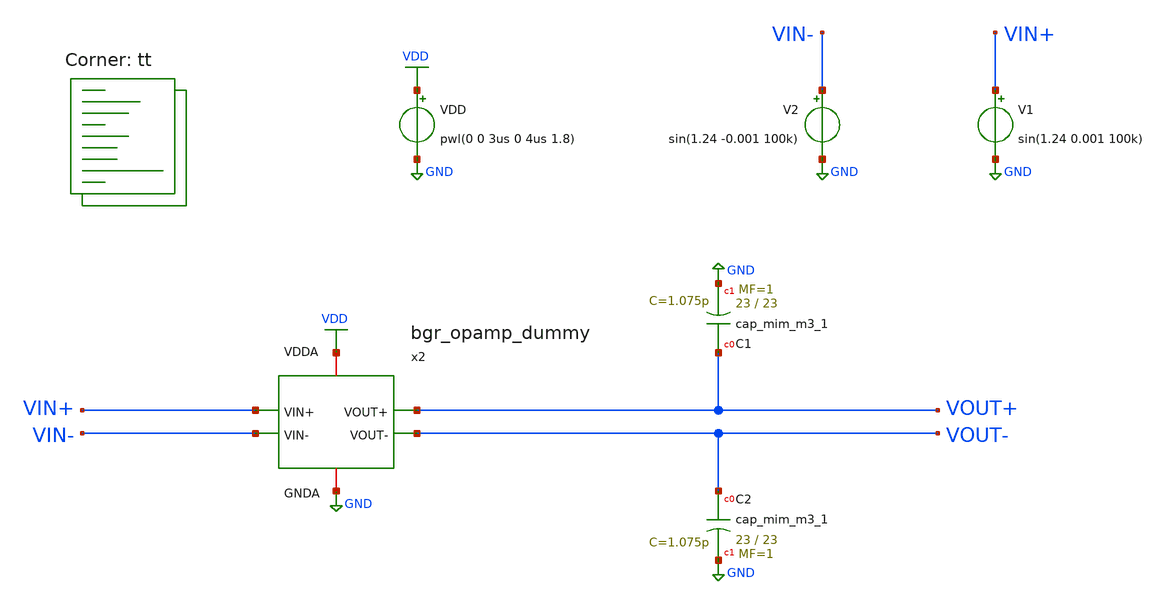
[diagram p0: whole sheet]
** sch_path: projects/opamp/xschem_ngspice/tb_bgr_opamp_dummy.sch
**.subckt tb_bgr_opamp_dummy
VDD VDD GND pwl(0 0 3us 0 4us 1.8)
V2 VIN- GND sin(1.24 -0.001 100k)
V1 VIN+ GND sin(1.24 0.001 100k)
XC1 VOUT+ GND sky130_fd_pr__cap_mim_m3_1 W=23 L=23 MF=1 m=1
XC2 VOUT- GND sky130_fd_pr__cap_mim_m3_1 W=23 L=23 MF=1 m=1
x2 VDD GND VOUT+ VOUT- VIN+ VIN- bgr_opamp_dummy
**** begin user architecture code
.lib $::SKYWATER_MODELS/sky130.lib.spice tt




.option method=gear
.option wnflag=1
.option savecurrents

.save @m.x2.xm25.msky130_fd_pr__nfet_01v8[vth] @m.x2.xm26.msky130_fd_pr__pfet_01v8[vth] @m.x2.xm27.msky130_fd_pr__nfet_01v8[vth] @m.x2.xm28.msky130_fd_pr__pfet_01v8[vth] v(vout+)  v(vout-)  v(vin+)  v(vin-)   v(x2.v_err_amp_ref) v(x2.x)  v(x2.y)  v(x2.vb1)  v(x2.vb2)  v(x2.vb3) v(x2.v_cmfb_s1) v(x2.v_cmfb_s2) v(x2.v_cmfb_s3) v(x2.v_cmfb_s4)   v(x2.v_tot)

* .ic v(v_top) = 1.8

.control

  * let runs=3
  * let run=1

  * dowhile run <= runs
    * save v(vout+) v(vout-) v(vin+) v(vin-) v(v_err_amp_ref) v(x2.x) v(x2.y) v(x2.vb1) v(x2.vb2)
+ v(x2.vb3) v(x2.v_tot)
    save all
    remzerovec
    set appendwrite
    * dc temp -40 120 10 VDD 0 4.0 0.2
    * dc VDD 0 2.0 0.02 temp -40 120 40
    * dc V5 0 0.01 0.0001
    tran 2n 30u
    * tran 1p 3n
    * tran 0.1ns 30us
    * ac dec 40 1 10T
    write tb_bgr_opamp_dummy.raw
    * write tb_bgr_opamp_dummy_2.raw
    * write tb_bgr_opamp_dummy_3.raw
    * write tb_bgr_opamp_dummy_4.raw
    * write tb_bgr_opamp_dummy_5.raw
    * write tb_bgr_opamp_dummy_6.raw
    * write tb_bgr_opamp_dummy_mc.raw
    * write tb_bgr_opamp_dummy_tt_mm.raw
    * write tb_bgr_opamp_dummy_AC.raw
    * reset
    * let run = run + 1
  * end
.endc




**** end user architecture code
**.ends

* expanding   symbol:  bgr_opamp_dummy.sym # of pins=6
** sym_path: projects/opamp/xschem_ngspice/bgr_opamp_dummy.sym
** sch_path: projects/opamp/xschem_ngspice/bgr_opamp_dummy.sch
.subckt bgr_opamp_dummy VDDA GNDA VOUT+ VOUT- VIN+ VIN-
*.ipin VIN-
*.ipin VIN+
*.opin VOUT+
*.opin VOUT-
*.iopin GNDA
*.iopin VDDA
XM7 VD1 VIN- V_p GNDA sky130_fd_pr__nfet_01v8 L=0.15 W=15 nf=1 ad='int((nf+1)/2) * W/nf * 0.29' as='int((nf+2)/2) * W/nf * 0.29'
+ pd='2*int((nf+1)/2) * (W/nf + 0.29)' ps='2*int((nf+2)/2) * (W/nf + 0.29)' nrd='0.29 / W' nrs='0.29 / W'
+ sa=0 sb=0 sd=0 mult=1 m=1
XM8 VD2 VIN+ V_p GNDA sky130_fd_pr__nfet_01v8 L=0.15 W=15 nf=1 ad='int((nf+1)/2) * W/nf * 0.29' as='int((nf+2)/2) * W/nf * 0.29'
+ pd='2*int((nf+1)/2) * (W/nf + 0.29)' ps='2*int((nf+2)/2) * (W/nf + 0.29)' nrd='0.29 / W' nrs='0.29 / W'
+ sa=0 sb=0 sd=0 mult=1 m=1
XM9 X Vb1 VD1 GNDA sky130_fd_pr__nfet_01v8 L=0.15 W=15 nf=1 ad='int((nf+1)/2) * W/nf * 0.29' as='int((nf+2)/2) * W/nf * 0.29'
+ pd='2*int((nf+1)/2) * (W/nf + 0.29)' ps='2*int((nf+2)/2) * (W/nf + 0.29)' nrd='0.29 / W' nrs='0.29 / W'
+ sa=0 sb=0 sd=0 mult=1 m=1
XM10 Y Vb1 VD2 GNDA sky130_fd_pr__nfet_01v8 L=0.15 W=15 nf=1 ad='int((nf+1)/2) * W/nf * 0.29' as='int((nf+2)/2) * W/nf * 0.29'
+ pd='2*int((nf+1)/2) * (W/nf + 0.29)' ps='2*int((nf+2)/2) * (W/nf + 0.29)' nrd='0.29 / W' nrs='0.29 / W'
+ sa=0 sb=0 sd=0 mult=1 m=1
XM11 X Vb2 VD3 VD3 sky130_fd_pr__pfet_01v8 L=0.2 W=35 nf=1 ad='int((nf+1)/2) * W/nf * 0.29' as='int((nf+2)/2) * W/nf * 0.29'
+ pd='2*int((nf+1)/2) * (W/nf + 0.29)' ps='2*int((nf+2)/2) * (W/nf + 0.29)' nrd='0.29 / W' nrs='0.29 / W'
+ sa=0 sb=0 sd=0 mult=1 m=1
XM12 Y Vb2 VD4 VD4 sky130_fd_pr__pfet_01v8 L=0.2 W=35 nf=1 ad='int((nf+1)/2) * W/nf * 0.29' as='int((nf+2)/2) * W/nf * 0.29'
+ pd='2*int((nf+1)/2) * (W/nf + 0.29)' ps='2*int((nf+2)/2) * (W/nf + 0.29)' nrd='0.29 / W' nrs='0.29 / W'
+ sa=0 sb=0 sd=0 mult=1 m=1
XM13 VD3 Vb3 VDDA VDDA sky130_fd_pr__pfet_01v8 L=0.2 W=35 nf=1 ad='int((nf+1)/2) * W/nf * 0.29' as='int((nf+2)/2) * W/nf * 0.29'
+ pd='2*int((nf+1)/2) * (W/nf + 0.29)' ps='2*int((nf+2)/2) * (W/nf + 0.29)' nrd='0.29 / W' nrs='0.29 / W'
+ sa=0 sb=0 sd=0 mult=1 m=1
XM14 VD4 Vb3 VDDA VDDA sky130_fd_pr__pfet_01v8 L=0.2 W=35 nf=1 ad='int((nf+1)/2) * W/nf * 0.29' as='int((nf+2)/2) * W/nf * 0.29'
+ pd='2*int((nf+1)/2) * (W/nf + 0.29)' ps='2*int((nf+2)/2) * (W/nf + 0.29)' nrd='0.29 / W' nrs='0.29 / W'
+ sa=0 sb=0 sd=0 mult=1 m=1
XM15 V_p V_tail_gate GNDA GNDA sky130_fd_pr__nfet_01v8 L=0.15 W=2.5 nf=1 ad='int((nf+1)/2) * W/nf * 0.29'
+ as='int((nf+2)/2) * W/nf * 0.29' pd='2*int((nf+1)/2) * (W/nf + 0.29)' ps='2*int((nf+2)/2) * (W/nf + 0.29)'
+ nrd='0.29 / W' nrs='0.29 / W' sa=0 sb=0 sd=0 mult=18 m=18
XM16 V_p_mir V_tail_gate GNDA GNDA sky130_fd_pr__nfet_01v8 L=0.15 W=2.5 nf=1 ad='int((nf+1)/2) * W/nf * 0.29'
+ as='int((nf+2)/2) * W/nf * 0.29' pd='2*int((nf+1)/2) * (W/nf + 0.29)' ps='2*int((nf+2)/2) * (W/nf + 0.29)'
+ nrd='0.29 / W' nrs='0.29 / W' sa=0 sb=0 sd=0 mult=2 m=2
XM17 V_tail_gate VIN+ V_p_mir GNDA sky130_fd_pr__nfet_01v8 L=0.15 W=1.5 nf=1 ad='int((nf+1)/2) * W/nf * 0.29'
+ as='int((nf+2)/2) * W/nf * 0.29' pd='2*int((nf+1)/2) * (W/nf + 0.29)' ps='2*int((nf+2)/2) * (W/nf + 0.29)'
+ nrd='0.29 / W' nrs='0.29 / W' sa=0 sb=0 sd=0 mult=1 m=1
XM18 V_tail_gate VIN- V_p_mir GNDA sky130_fd_pr__nfet_01v8 L=0.15 W=1.5 nf=1 ad='int((nf+1)/2) * W/nf * 0.29'
+ as='int((nf+2)/2) * W/nf * 0.29' pd='2*int((nf+1)/2) * (W/nf + 0.29)' ps='2*int((nf+2)/2) * (W/nf + 0.29)'
+ nrd='0.29 / W' nrs='0.29 / W' sa=0 sb=0 sd=0 mult=1 m=1
XM19 Vb1 Vb1 V_p GNDA sky130_fd_pr__nfet_01v8 L=2.9 W=1 nf=1 ad='int((nf+1)/2) * W/nf * 0.29' as='int((nf+2)/2) * W/nf * 0.29'
+ pd='2*int((nf+1)/2) * (W/nf + 0.29)' ps='2*int((nf+2)/2) * (W/nf + 0.29)' nrd='0.29 / W' nrs='0.29 / W'
+ sa=0 sb=0 sd=0 mult=1 m=1
XM25 VDDA X V_CMFB_S2 GNDA sky130_fd_pr__nfet_01v8 L=0.15 W=30 nf=1 ad='int((nf+1)/2) * W/nf * 0.29'
+ as='int((nf+2)/2) * W/nf * 0.29' pd='2*int((nf+1)/2) * (W/nf + 0.29)' ps='2*int((nf+2)/2) * (W/nf + 0.29)'
+ nrd='0.29 / W' nrs='0.29 / W' sa=0 sb=0 sd=0 mult=1 m=1
XM26 GNDA X V_CMFB_S1 VDDA sky130_fd_pr__pfet_01v8 L=0.15 W=20 nf=1 ad='int((nf+1)/2) * W/nf * 0.29'
+ as='int((nf+2)/2) * W/nf * 0.29' pd='2*int((nf+1)/2) * (W/nf + 0.29)' ps='2*int((nf+2)/2) * (W/nf + 0.29)'
+ nrd='0.29 / W' nrs='0.29 / W' sa=0 sb=0 sd=0 mult=1 m=1
XR10 V_CMFB_S1 V_tot GNDA sky130_fd_pr__res_xhigh_po_0p35 L=3.5 mult=1 m=1
XR11 V_CMFB_S2 V_tot GNDA sky130_fd_pr__res_xhigh_po_0p35 L=3.5 mult=1 m=1
XR12 V_CMFB_S3 V_tot GNDA sky130_fd_pr__res_xhigh_po_0p35 L=3.5 mult=1 m=1
XR13 V_CMFB_S4 V_tot GNDA sky130_fd_pr__res_xhigh_po_0p35 L=3.5 mult=1 m=1
XM27 VDDA Y V_CMFB_S4 GNDA sky130_fd_pr__nfet_01v8 L=0.15 W=30 nf=1 ad='int((nf+1)/2) * W/nf * 0.29'
+ as='int((nf+2)/2) * W/nf * 0.29' pd='2*int((nf+1)/2) * (W/nf + 0.29)' ps='2*int((nf+2)/2) * (W/nf + 0.29)'
+ nrd='0.29 / W' nrs='0.29 / W' sa=0 sb=0 sd=0 mult=1 m=1
XM28 GNDA Y V_CMFB_S3 VDDA sky130_fd_pr__pfet_01v8 L=0.15 W=20 nf=1 ad='int((nf+1)/2) * W/nf * 0.29'
+ as='int((nf+2)/2) * W/nf * 0.29' pd='2*int((nf+1)/2) * (W/nf + 0.29)' ps='2*int((nf+2)/2) * (W/nf + 0.29)'
+ nrd='0.29 / W' nrs='0.29 / W' sa=0 sb=0 sd=0 mult=1 m=1
XM29 err_amp_mir V_tot V_err_p VDDA sky130_fd_pr__pfet_01v8 L=0.15 W=2.5 nf=1 ad='int((nf+1)/2) * W/nf * 0.29'
+ as='int((nf+2)/2) * W/nf * 0.29' pd='2*int((nf+1)/2) * (W/nf + 0.29)' ps='2*int((nf+2)/2) * (W/nf + 0.29)'
+ nrd='0.29 / W' nrs='0.29 / W' sa=0 sb=0 sd=0 mult=1 m=1
XM30 err_amp_out V_err_amp_ref V_err_p VDDA sky130_fd_pr__pfet_01v8 L=0.15 W=2.5 nf=1 ad='int((nf+1)/2) * W/nf * 0.29'
+ as='int((nf+2)/2) * W/nf * 0.29' pd='2*int((nf+1)/2) * (W/nf + 0.29)' ps='2*int((nf+2)/2) * (W/nf + 0.29)'
+ nrd='0.29 / W' nrs='0.29 / W' sa=0 sb=0 sd=0 mult=1 m=1
XM31 err_amp_mir err_amp_mir GNDA GNDA sky130_fd_pr__nfet_01v8 L=0.15 W=2.5 nf=1 ad='int((nf+1)/2) * W/nf * 0.29'
+ as='int((nf+2)/2) * W/nf * 0.29' pd='2*int((nf+1)/2) * (W/nf + 0.29)' ps='2*int((nf+2)/2) * (W/nf + 0.29)'
+ nrd='0.29 / W' nrs='0.29 / W' sa=0 sb=0 sd=0 mult=1 m=1
XM32 err_amp_out err_amp_mir GNDA GNDA sky130_fd_pr__nfet_01v8 L=0.15 W=2.5 nf=1 ad='int((nf+1)/2) * W/nf * 0.29'
+ as='int((nf+2)/2) * W/nf * 0.29' pd='2*int((nf+1)/2) * (W/nf + 0.29)' ps='2*int((nf+2)/2) * (W/nf + 0.29)'
+ nrd='0.29 / W' nrs='0.29 / W' sa=0 sb=0 sd=0 mult=1 m=1
XM33 V_err_p V_err_gate VDDA VDDA sky130_fd_pr__pfet_01v8 L=0.15 W=5.0 nf=2 ad='int((nf+1)/2) * W/nf * 0.29'
+ as='int((nf+2)/2) * W/nf * 0.29' pd='2*int((nf+1)/2) * (W/nf + 0.29)' ps='2*int((nf+2)/2) * (W/nf + 0.29)'
+ nrd='0.29 / W' nrs='0.29 / W' sa=0 sb=0 sd=0 mult=1 m=1
XM34 V_err_gate V_tot V_err_mir_p VDDA sky130_fd_pr__pfet_01v8 L=0.15 W=2.5 nf=1 ad='int((nf+1)/2) * W/nf * 0.29'
+ as='int((nf+2)/2) * W/nf * 0.29' pd='2*int((nf+1)/2) * (W/nf + 0.29)' ps='2*int((nf+2)/2) * (W/nf + 0.29)'
+ nrd='0.29 / W' nrs='0.29 / W' sa=0 sb=0 sd=0 mult=1 m=1
XM35 V_err_gate V_err_amp_ref V_err_mir_p VDDA sky130_fd_pr__pfet_01v8 L=0.15 W=2.5 nf=1 ad='int((nf+1)/2) * W/nf * 0.29'
+ as='int((nf+2)/2) * W/nf * 0.29' pd='2*int((nf+1)/2) * (W/nf + 0.29)' ps='2*int((nf+2)/2) * (W/nf + 0.29)'
+ nrd='0.29 / W' nrs='0.29 / W' sa=0 sb=0 sd=0 mult=1 m=1
XM36 V_err_mir_p V_err_gate VDDA VDDA sky130_fd_pr__pfet_01v8 L=0.15 W=5.0 nf=2 ad='int((nf+1)/2) * W/nf * 0.29'
+ as='int((nf+2)/2) * W/nf * 0.29' pd='2*int((nf+1)/2) * (W/nf + 0.29)' ps='2*int((nf+2)/2) * (W/nf + 0.29)'
+ nrd='0.29 / W' nrs='0.29 / W' sa=0 sb=0 sd=0 mult=1 m=1
XM37 VOUT- V_b_2nd_stage GNDA GNDA sky130_fd_pr__nfet_01v8 L=0.6 W=28 nf=1 ad='int((nf+1)/2) * W/nf * 0.29'
+ as='int((nf+2)/2) * W/nf * 0.29' pd='2*int((nf+1)/2) * (W/nf + 0.29)' ps='2*int((nf+2)/2) * (W/nf + 0.29)'
+ nrd='0.29 / W' nrs='0.29 / W' sa=0 sb=0 sd=0 mult=1 m=1
XM38 VOUT+ V_b_2nd_stage GNDA GNDA sky130_fd_pr__nfet_01v8 L=0.6 W=28 nf=1 ad='int((nf+1)/2) * W/nf * 0.29'
+ as='int((nf+2)/2) * W/nf * 0.29' pd='2*int((nf+1)/2) * (W/nf + 0.29)' ps='2*int((nf+2)/2) * (W/nf + 0.29)'
+ nrd='0.29 / W' nrs='0.29 / W' sa=0 sb=0 sd=0 mult=1 m=1
XM39 VOUT- X VDDA VDDA sky130_fd_pr__pfet_01v8 L=0.15 W=60 nf=1 ad='int((nf+1)/2) * W/nf * 0.29' as='int((nf+2)/2) * W/nf * 0.29'
+ pd='2*int((nf+1)/2) * (W/nf + 0.29)' ps='2*int((nf+2)/2) * (W/nf + 0.29)' nrd='0.29 / W' nrs='0.29 / W'
+ sa=0 sb=0 sd=0 mult=1 m=1
XM40 VOUT+ Y VDDA VDDA sky130_fd_pr__pfet_01v8 L=0.15 W=60 nf=1 ad='int((nf+1)/2) * W/nf * 0.29' as='int((nf+2)/2) * W/nf * 0.29'
+ pd='2*int((nf+1)/2) * (W/nf + 0.29)' ps='2*int((nf+2)/2) * (W/nf + 0.29)' nrd='0.29 / W' nrs='0.29 / W'
+ sa=0 sb=0 sd=0 mult=1 m=1
XR22 VOUT- V_b_2nd_stage GNDA sky130_fd_pr__res_xhigh_po_0p35 L=5.25 mult=1 m=1
XR23 VOUT+ V_b_2nd_stage GNDA sky130_fd_pr__res_xhigh_po_0p35 L=5.25 mult=1 m=1
XM41 V_p err_amp_out GNDA GNDA sky130_fd_pr__nfet_01v8 L=0.15 W=2.5 nf=1 ad='int((nf+1)/2) * W/nf * 0.29'
+ as='int((nf+2)/2) * W/nf * 0.29' pd='2*int((nf+1)/2) * (W/nf + 0.29)' ps='2*int((nf+2)/2) * (W/nf + 0.29)'
+ nrd='0.29 / W' nrs='0.29 / W' sa=0 sb=0 sd=0 mult=1 m=1
XC6 VOUT+ cap_res_Y sky130_fd_pr__cap_mim_m3_1 W=2 L=2 MF=138 m=138
XC7 VOUT- cap_res_X sky130_fd_pr__cap_mim_m3_1 W=2 L=2 MF=138 m=138
XM21 GNDA GNDA GNDA GNDA sky130_fd_pr__nfet_01v8 L=0.15 W=2.5 nf=1 ad='int((nf+1)/2) * W/nf * 0.29' as='int((nf+2)/2) * W/nf * 0.29'
+ pd='2*int((nf+1)/2) * (W/nf + 0.29)' ps='2*int((nf+2)/2) * (W/nf + 0.29)' nrd='0.29 / W' nrs='0.29 / W'
+ sa=0 sb=0 sd=0 mult=1 m=1
XM22 V_p GNDA GNDA GNDA sky130_fd_pr__nfet_01v8 L=0.15 W=2.5 nf=1 ad='int((nf+1)/2) * W/nf * 0.29' as='int((nf+2)/2) * W/nf * 0.29'
+ pd='2*int((nf+1)/2) * (W/nf + 0.29)' ps='2*int((nf+2)/2) * (W/nf + 0.29)' nrd='0.29 / W' nrs='0.29 / W'
+ sa=0 sb=0 sd=0 mult=1 m=1
XM23 V_tail_gate GNDA GNDA GNDA sky130_fd_pr__nfet_01v8 L=0.15 W=3.0 nf=2 ad='int((nf+1)/2) * W/nf * 0.29'
+ as='int((nf+2)/2) * W/nf * 0.29' pd='2*int((nf+1)/2) * (W/nf + 0.29)' ps='2*int((nf+2)/2) * (W/nf + 0.29)'
+ nrd='0.29 / W' nrs='0.29 / W' sa=0 sb=0 sd=0 mult=1 m=1
XM24 VD1 GNDA GNDA GNDA sky130_fd_pr__nfet_01v8 L=0.15 W=3.0 nf=2 ad='int((nf+1)/2) * W/nf * 0.29' as='int((nf+2)/2) * W/nf * 0.29'
+ pd='2*int((nf+1)/2) * (W/nf + 0.29)' ps='2*int((nf+2)/2) * (W/nf + 0.29)' nrd='0.29 / W' nrs='0.29 / W'
+ sa=0 sb=0 sd=0 mult=1 m=1
XM46 VD2 GNDA GNDA GNDA sky130_fd_pr__nfet_01v8 L=0.15 W=3.0 nf=2 ad='int((nf+1)/2) * W/nf * 0.29' as='int((nf+2)/2) * W/nf * 0.29'
+ pd='2*int((nf+1)/2) * (W/nf + 0.29)' ps='2*int((nf+2)/2) * (W/nf + 0.29)' nrd='0.29 / W' nrs='0.29 / W'
+ sa=0 sb=0 sd=0 mult=1 m=1
XM47 Y GNDA GNDA GNDA sky130_fd_pr__nfet_01v8 L=0.15 W=3.0 nf=2 ad='int((nf+1)/2) * W/nf * 0.29' as='int((nf+2)/2) * W/nf * 0.29'
+ pd='2*int((nf+1)/2) * (W/nf + 0.29)' ps='2*int((nf+2)/2) * (W/nf + 0.29)' nrd='0.29 / W' nrs='0.29 / W'
+ sa=0 sb=0 sd=0 mult=1 m=1
XM48 VD3 VDDA VDDA VDDA sky130_fd_pr__pfet_01v8 L=0.2 W=7.0 nf=2 ad='int((nf+1)/2) * W/nf * 0.29' as='int((nf+2)/2) * W/nf * 0.29'
+ pd='2*int((nf+1)/2) * (W/nf + 0.29)' ps='2*int((nf+2)/2) * (W/nf + 0.29)' nrd='0.29 / W' nrs='0.29 / W'
+ sa=0 sb=0 sd=0 mult=1 m=1
XM49 Y VD4 VD4 VD4 sky130_fd_pr__pfet_01v8 L=0.2 W=7.0 nf=2 ad='int((nf+1)/2) * W/nf * 0.29' as='int((nf+2)/2) * W/nf * 0.29'
+ pd='2*int((nf+1)/2) * (W/nf + 0.29)' ps='2*int((nf+2)/2) * (W/nf + 0.29)' nrd='0.29 / W' nrs='0.29 / W'
+ sa=0 sb=0 sd=0 mult=1 m=1
XM52 X VD3 VD3 VD3 sky130_fd_pr__pfet_01v8 L=0.2 W=7.0 nf=2 ad='int((nf+1)/2) * W/nf * 0.29' as='int((nf+2)/2) * W/nf * 0.29'
+ pd='2*int((nf+1)/2) * (W/nf + 0.29)' ps='2*int((nf+2)/2) * (W/nf + 0.29)' nrd='0.29 / W' nrs='0.29 / W'
+ sa=0 sb=0 sd=0 mult=1 m=1
XM58 V_err_p VDDA VDDA VDDA sky130_fd_pr__pfet_01v8 L=0.15 W=1.0 nf=2 ad='int((nf+1)/2) * W/nf * 0.29'
+ as='int((nf+2)/2) * W/nf * 0.29' pd='2*int((nf+1)/2) * (W/nf + 0.29)' ps='2*int((nf+2)/2) * (W/nf + 0.29)'
+ nrd='0.29 / W' nrs='0.29 / W' sa=0 sb=0 sd=0 mult=1 m=1
XM59 err_amp_out VDDA VDDA VDDA sky130_fd_pr__pfet_01v8 L=0.15 W=0.5 nf=1 ad='int((nf+1)/2) * W/nf * 0.29'
+ as='int((nf+2)/2) * W/nf * 0.29' pd='2*int((nf+1)/2) * (W/nf + 0.29)' ps='2*int((nf+2)/2) * (W/nf + 0.29)'
+ nrd='0.29 / W' nrs='0.29 / W' sa=0 sb=0 sd=0 mult=1 m=1
XM60 V_err_gate VDDA VDDA VDDA sky130_fd_pr__pfet_01v8 L=0.15 W=1.0 nf=2 ad='int((nf+1)/2) * W/nf * 0.29'
+ as='int((nf+2)/2) * W/nf * 0.29' pd='2*int((nf+1)/2) * (W/nf + 0.29)' ps='2*int((nf+2)/2) * (W/nf + 0.29)'
+ nrd='0.29 / W' nrs='0.29 / W' sa=0 sb=0 sd=0 mult=1 m=1
XM61 err_amp_mir VDDA VDDA VDDA sky130_fd_pr__pfet_01v8 L=0.15 W=0.5 nf=1 ad='int((nf+1)/2) * W/nf * 0.29'
+ as='int((nf+2)/2) * W/nf * 0.29' pd='2*int((nf+1)/2) * (W/nf + 0.29)' ps='2*int((nf+2)/2) * (W/nf + 0.29)'
+ nrd='0.29 / W' nrs='0.29 / W' sa=0 sb=0 sd=0 mult=1 m=1
XM62 GNDA VDDA VDDA VDDA sky130_fd_pr__pfet_01v8 L=0.15 W=4 nf=2 ad='int((nf+1)/2) * W/nf * 0.29' as='int((nf+2)/2) * W/nf * 0.29'
+ pd='2*int((nf+1)/2) * (W/nf + 0.29)' ps='2*int((nf+2)/2) * (W/nf + 0.29)' nrd='0.29 / W' nrs='0.29 / W'
+ sa=0 sb=0 sd=0 mult=1 m=1
XM63 GNDA VDDA VDDA VDDA sky130_fd_pr__pfet_01v8 L=0.15 W=4 nf=2 ad='int((nf+1)/2) * W/nf * 0.29' as='int((nf+2)/2) * W/nf * 0.29'
+ pd='2*int((nf+1)/2) * (W/nf + 0.29)' ps='2*int((nf+2)/2) * (W/nf + 0.29)' nrd='0.29 / W' nrs='0.29 / W'
+ sa=0 sb=0 sd=0 mult=1 m=1
XM64 VDDA GNDA GNDA GNDA sky130_fd_pr__nfet_01v8 L=0.15 W=6 nf=2 ad='int((nf+1)/2) * W/nf * 0.29' as='int((nf+2)/2) * W/nf * 0.29'
+ pd='2*int((nf+1)/2) * (W/nf + 0.29)' ps='2*int((nf+2)/2) * (W/nf + 0.29)' nrd='0.29 / W' nrs='0.29 / W'
+ sa=0 sb=0 sd=0 mult=1 m=1
XM65 VDDA GNDA GNDA GNDA sky130_fd_pr__nfet_01v8 L=0.15 W=6 nf=2 ad='int((nf+1)/2) * W/nf * 0.29' as='int((nf+2)/2) * W/nf * 0.29'
+ pd='2*int((nf+1)/2) * (W/nf + 0.29)' ps='2*int((nf+2)/2) * (W/nf + 0.29)' nrd='0.29 / W' nrs='0.29 / W'
+ sa=0 sb=0 sd=0 mult=1 m=1
XM66 VOUT+ GNDA GNDA GNDA sky130_fd_pr__nfet_01v8 L=0.6 W=14 nf=2 ad='int((nf+1)/2) * W/nf * 0.29' as='int((nf+2)/2) * W/nf * 0.29'
+ pd='2*int((nf+1)/2) * (W/nf + 0.29)' ps='2*int((nf+2)/2) * (W/nf + 0.29)' nrd='0.29 / W' nrs='0.29 / W'
+ sa=0 sb=0 sd=0 mult=1 m=1
XM68 VOUT- VDDA VDDA VDDA sky130_fd_pr__pfet_01v8 L=0.15 W=12 nf=2 ad='int((nf+1)/2) * W/nf * 0.29' as='int((nf+2)/2) * W/nf * 0.29'
+ pd='2*int((nf+1)/2) * (W/nf + 0.29)' ps='2*int((nf+2)/2) * (W/nf + 0.29)' nrd='0.29 / W' nrs='0.29 / W'
+ sa=0 sb=0 sd=0 mult=1 m=1
XM69 VOUT- GNDA GNDA GNDA sky130_fd_pr__nfet_01v8 L=0.6 W=14 nf=2 ad='int((nf+1)/2) * W/nf * 0.29' as='int((nf+2)/2) * W/nf * 0.29'
+ pd='2*int((nf+1)/2) * (W/nf + 0.29)' ps='2*int((nf+2)/2) * (W/nf + 0.29)' nrd='0.29 / W' nrs='0.29 / W'
+ sa=0 sb=0 sd=0 mult=1 m=1
XM67 VOUT+ VDDA VDDA VDDA sky130_fd_pr__pfet_01v8 L=0.15 W=12 nf=2 ad='int((nf+1)/2) * W/nf * 0.29' as='int((nf+2)/2) * W/nf * 0.29'
+ pd='2*int((nf+1)/2) * (W/nf + 0.29)' ps='2*int((nf+2)/2) * (W/nf + 0.29)' nrd='0.29 / W' nrs='0.29 / W'
+ sa=0 sb=0 sd=0 mult=1 m=1
XR1 cap_res_X X GNDA sky130_fd_pr__res_high_po_1p41 L=1.41 mult=1 m=1
XR2 cap_res_Y Y GNDA sky130_fd_pr__res_high_po_1p41 L=1.41 mult=1 m=1
XM20 err_amp_mir GNDA GNDA GNDA sky130_fd_pr__nfet_01v8 L=0.15 W=0.5 nf=1 ad='int((nf+1)/2) * W/nf * 0.29'
+ as='int((nf+2)/2) * W/nf * 0.29' pd='2*int((nf+1)/2) * (W/nf + 0.29)' ps='2*int((nf+2)/2) * (W/nf + 0.29)'
+ nrd='0.29 / W' nrs='0.29 / W' sa=0 sb=0 sd=0 mult=1 m=1
XM42 err_amp_out GNDA GNDA GNDA sky130_fd_pr__nfet_01v8 L=0.15 W=0.5 nf=1 ad='int((nf+1)/2) * W/nf * 0.29'
+ as='int((nf+2)/2) * W/nf * 0.29' pd='2*int((nf+1)/2) * (W/nf + 0.29)' ps='2*int((nf+2)/2) * (W/nf + 0.29)'
+ nrd='0.29 / W' nrs='0.29 / W' sa=0 sb=0 sd=0 mult=1 m=1
XM44 X GNDA GNDA GNDA sky130_fd_pr__nfet_01v8 L=0.15 W=3.0 nf=2 ad='int((nf+1)/2) * W/nf * 0.29' as='int((nf+2)/2) * W/nf * 0.29'
+ pd='2*int((nf+1)/2) * (W/nf + 0.29)' ps='2*int((nf+2)/2) * (W/nf + 0.29)' nrd='0.29 / W' nrs='0.29 / W'
+ sa=0 sb=0 sd=0 mult=1 m=1
XM45 V_err_amp_ref V_TOP VDDA VDDA sky130_fd_pr__pfet_01v8 L=0.5 W=12 nf=4 ad='int((nf+1)/2) * W/nf * 0.29'
+ as='int((nf+2)/2) * W/nf * 0.29' pd='2*int((nf+1)/2) * (W/nf + 0.29)' ps='2*int((nf+2)/2) * (W/nf + 0.29)'
+ nrd='0.29 / W' nrs='0.29 / W' sa=0 sb=0 sd=0 mult=1 m=1
XR4 GNDA V_err_amp_ref GNDA sky130_fd_pr__res_xhigh_po_0p35 L=12.7 mult=1 m=1
XR5 GNDA V_CUR_REF_REG GNDA sky130_fd_pr__res_xhigh_po_0p35 L=12 mult=1 m=1
XM50 V_CUR_REF_REG PFET_GATE_10uA VDDA VDDA sky130_fd_pr__pfet_01v8 L=0.15 W=1 nf=1 ad='int((nf+1)/2) * W/nf * 0.29'
+ as='int((nf+2)/2) * W/nf * 0.29' pd='2*int((nf+1)/2) * (W/nf + 0.29)' ps='2*int((nf+2)/2) * (W/nf + 0.29)'
+ nrd='0.29 / W' nrs='0.29 / W' sa=0 sb=0 sd=0 mult=1 m=1
XC1 V_TOP VDDA sky130_fd_pr__cap_mim_m3_1 W=2 L=2 MF=20 m=20
XQ1 GNDA GNDA bgr_Vin- sky130_fd_pr__pnp_05v5_W3p40L3p40 m=1
XQ2 GNDA GNDA Vbe2 sky130_fd_pr__pnp_05v5_W3p40L3p40 m=8
XM51 bgr_Vin- V_TOP VDDA VDDA sky130_fd_pr__pfet_01v8 L=0.5 W=12 nf=4 ad='int((nf+1)/2) * W/nf * 0.29'
+ as='int((nf+2)/2) * W/nf * 0.29' pd='2*int((nf+1)/2) * (W/nf + 0.29)' ps='2*int((nf+2)/2) * (W/nf + 0.29)'
+ nrd='0.29 / W' nrs='0.29 / W' sa=0 sb=0 sd=0 mult=1 m=1
XM53 bgr_Vin+ V_TOP VDDA VDDA sky130_fd_pr__pfet_01v8 L=0.5 W=12 nf=4 ad='int((nf+1)/2) * W/nf * 0.29'
+ as='int((nf+2)/2) * W/nf * 0.29' pd='2*int((nf+1)/2) * (W/nf + 0.29)' ps='2*int((nf+2)/2) * (W/nf + 0.29)'
+ nrd='0.29 / W' nrs='0.29 / W' sa=0 sb=0 sd=0 mult=1 m=1
XR3 Vbe2 bgr_Vin+ GNDA sky130_fd_pr__res_xhigh_po_0p35 L=2.3 mult=1 m=1
XR6 GNDA bgr_Vin+ GNDA sky130_fd_pr__res_xhigh_po_0p35 L=18 mult=1 m=1
XR7 GNDA bgr_Vin- GNDA sky130_fd_pr__res_xhigh_po_0p35 L=18 mult=1 m=1
XM54 START_UP START_UP START_UP_NFET1 GNDA sky130_fd_pr__nfet_01v8 L=10 W=1 nf=1 ad='int((nf+1)/2) * W/nf * 0.29'
+ as='int((nf+2)/2) * W/nf * 0.29' pd='2*int((nf+1)/2) * (W/nf + 0.29)' ps='2*int((nf+2)/2) * (W/nf + 0.29)'
+ nrd='0.29 / W' nrs='0.29 / W' sa=0 sb=0 sd=0 mult=1 m=1
XM55 START_UP V_TOP VDDA VDDA sky130_fd_pr__pfet_01v8 L=0.5 W=12 nf=4 ad='int((nf+1)/2) * W/nf * 0.29'
+ as='int((nf+2)/2) * W/nf * 0.29' pd='2*int((nf+1)/2) * (W/nf + 0.29)' ps='2*int((nf+2)/2) * (W/nf + 0.29)'
+ nrd='0.29 / W' nrs='0.29 / W' sa=0 sb=0 sd=0 mult=1 m=1
XM56 bgr_Vin- START_UP V_TOP VDDA sky130_fd_pr__pfet_01v8 L=0.15 W=2 nf=2 ad='int((nf+1)/2) * W/nf * 0.29'
+ as='int((nf+2)/2) * W/nf * 0.29' pd='2*int((nf+1)/2) * (W/nf + 0.29)' ps='2*int((nf+2)/2) * (W/nf + 0.29)'
+ nrd='0.29 / W' nrs='0.29 / W' sa=0 sb=0 sd=0 mult=1 m=1
XM57 START_UP_NFET1 START_UP_NFET1 GNDA GNDA sky130_fd_pr__nfet_01v8 L=10 W=1 nf=1 ad='int((nf+1)/2) * W/nf * 0.29'
+ as='int((nf+2)/2) * W/nf * 0.29' pd='2*int((nf+1)/2) * (W/nf + 0.29)' ps='2*int((nf+2)/2) * (W/nf + 0.29)'
+ nrd='0.29 / W' nrs='0.29 / W' sa=0 sb=0 sd=0 mult=1 m=1
x1 VDDA V_TOP bgr_Vin- bgr_Vin+ GNDA opamp_bandgap_2
x2 VDDA PFET_GATE_10uA V_err_amp_ref V_CUR_REF_REG GNDA opamp_bandgap_2
XM70 NFET_GATE_10uA PFET_GATE_10uA VDDA VDDA sky130_fd_pr__pfet_01v8 L=0.15 W=1 nf=1 ad='int((nf+1)/2) * W/nf * 0.29'
+ as='int((nf+2)/2) * W/nf * 0.29' pd='2*int((nf+1)/2) * (W/nf + 0.29)' ps='2*int((nf+2)/2) * (W/nf + 0.29)'
+ nrd='0.29 / W' nrs='0.29 / W' sa=0 sb=0 sd=0 mult=1 m=1
XM71 NFET_GATE_10uA NFET_GATE_10uA GNDA GNDA sky130_fd_pr__nfet_01v8 L=0.15 W=1 nf=1 ad='int((nf+1)/2) * W/nf * 0.29'
+ as='int((nf+2)/2) * W/nf * 0.29' pd='2*int((nf+1)/2) * (W/nf + 0.29)' ps='2*int((nf+2)/2) * (W/nf + 0.29)'
+ nrd='0.29 / W' nrs='0.29 / W' sa=0 sb=0 sd=0 mult=1 m=1
XM72 Vb2 NFET_GATE_10uA GNDA GNDA sky130_fd_pr__nfet_01v8 L=0.15 W=1 nf=1 ad='int((nf+1)/2) * W/nf * 0.29'
+ as='int((nf+2)/2) * W/nf * 0.29' pd='2*int((nf+1)/2) * (W/nf + 0.29)' ps='2*int((nf+2)/2) * (W/nf + 0.29)'
+ nrd='0.29 / W' nrs='0.29 / W' sa=0 sb=0 sd=0 mult=6 m=6
XM73 Vb3 NFET_GATE_10uA GNDA GNDA sky130_fd_pr__nfet_01v8 L=0.15 W=1 nf=1 ad='int((nf+1)/2) * W/nf * 0.29'
+ as='int((nf+2)/2) * W/nf * 0.29' pd='2*int((nf+1)/2) * (W/nf + 0.29)' ps='2*int((nf+2)/2) * (W/nf + 0.29)'
+ nrd='0.29 / W' nrs='0.29 / W' sa=0 sb=0 sd=0 mult=5 m=5
XM74 Vb1 PFET_GATE_10uA VDDA VDDA sky130_fd_pr__pfet_01v8 L=0.15 W=1 nf=1 ad='int((nf+1)/2) * W/nf * 0.29'
+ as='int((nf+2)/2) * W/nf * 0.29' pd='2*int((nf+1)/2) * (W/nf + 0.29)' ps='2*int((nf+2)/2) * (W/nf + 0.29)'
+ nrd='0.29 / W' nrs='0.29 / W' sa=0 sb=0 sd=0 mult=2 m=2
XM75 V_err_gate NFET_GATE_10uA GNDA GNDA sky130_fd_pr__nfet_01v8 L=0.15 W=1 nf=1 ad='int((nf+1)/2) * W/nf * 0.29'
+ as='int((nf+2)/2) * W/nf * 0.29' pd='2*int((nf+1)/2) * (W/nf + 0.29)' ps='2*int((nf+2)/2) * (W/nf + 0.29)'
+ nrd='0.29 / W' nrs='0.29 / W' sa=0 sb=0 sd=0 mult=2 m=2
XM76 V_CMFB_S2 NFET_GATE_10uA GNDA GNDA sky130_fd_pr__nfet_01v8 L=0.15 W=1 nf=1 ad='int((nf+1)/2) * W/nf * 0.29'
+ as='int((nf+2)/2) * W/nf * 0.29' pd='2*int((nf+1)/2) * (W/nf + 0.29)' ps='2*int((nf+2)/2) * (W/nf + 0.29)'
+ nrd='0.29 / W' nrs='0.29 / W' sa=0 sb=0 sd=0 mult=3 m=3
XM77 V_tail_gate PFET_GATE_10uA VDDA VDDA sky130_fd_pr__pfet_01v8 L=0.15 W=1 nf=1 ad='int((nf+1)/2) * W/nf * 0.29'
+ as='int((nf+2)/2) * W/nf * 0.29' pd='2*int((nf+1)/2) * (W/nf + 0.29)' ps='2*int((nf+2)/2) * (W/nf + 0.29)'
+ nrd='0.29 / W' nrs='0.29 / W' sa=0 sb=0 sd=0 mult=8 m=8
XM78 NFET_GATE_10uA VDDA VDDA VDDA sky130_fd_pr__pfet_01v8 L=0.15 W=1 nf=1 ad='int((nf+1)/2) * W/nf * 0.29'
+ as='int((nf+2)/2) * W/nf * 0.29' pd='2*int((nf+1)/2) * (W/nf + 0.29)' ps='2*int((nf+2)/2) * (W/nf + 0.29)'
+ nrd='0.29 / W' nrs='0.29 / W' sa=0 sb=0 sd=0 mult=1 m=1
XM79 NFET_GATE_10uA GNDA GNDA GNDA sky130_fd_pr__nfet_01v8 L=0.15 W=1 nf=1 ad='int((nf+1)/2) * W/nf * 0.29'
+ as='int((nf+2)/2) * W/nf * 0.29' pd='2*int((nf+1)/2) * (W/nf + 0.29)' ps='2*int((nf+2)/2) * (W/nf + 0.29)'
+ nrd='0.29 / W' nrs='0.29 / W' sa=0 sb=0 sd=0 mult=1 m=1
XM80 V_CUR_REF_REG VDDA VDDA VDDA sky130_fd_pr__pfet_01v8 L=0.15 W=1 nf=1 ad='int((nf+1)/2) * W/nf * 0.29'
+ as='int((nf+2)/2) * W/nf * 0.29' pd='2*int((nf+1)/2) * (W/nf + 0.29)' ps='2*int((nf+2)/2) * (W/nf + 0.29)'
+ nrd='0.29 / W' nrs='0.29 / W' sa=0 sb=0 sd=0 mult=1 m=1
XM81 Vb3 GNDA GNDA GNDA sky130_fd_pr__nfet_01v8 L=0.15 W=1 nf=1 ad='int((nf+1)/2) * W/nf * 0.29' as='int((nf+2)/2) * W/nf * 0.29'
+ pd='2*int((nf+1)/2) * (W/nf + 0.29)' ps='2*int((nf+2)/2) * (W/nf + 0.29)' nrd='0.29 / W' nrs='0.29 / W'
+ sa=0 sb=0 sd=0 mult=1 m=1
XM82 V_CMFB_S1 PFET_GATE_10uA VDDA VDDA sky130_fd_pr__pfet_01v8 L=0.15 W=1 nf=1 ad='int((nf+1)/2) * W/nf * 0.29'
+ as='int((nf+2)/2) * W/nf * 0.29' pd='2*int((nf+1)/2) * (W/nf + 0.29)' ps='2*int((nf+2)/2) * (W/nf + 0.29)'
+ nrd='0.29 / W' nrs='0.29 / W' sa=0 sb=0 sd=0 mult=4 m=4
XM83 V_err_amp_ref VDDA VDDA VDDA sky130_fd_pr__pfet_01v8 L=0.5 W=6 nf=2 ad='int((nf+1)/2) * W/nf * 0.29'
+ as='int((nf+2)/2) * W/nf * 0.29' pd='2*int((nf+1)/2) * (W/nf + 0.29)' ps='2*int((nf+2)/2) * (W/nf + 0.29)'
+ nrd='0.29 / W' nrs='0.29 / W' sa=0 sb=0 sd=0 mult=1 m=1
XM84 V_CMFB_S4 NFET_GATE_10uA GNDA GNDA sky130_fd_pr__nfet_01v8 L=0.15 W=1 nf=1 ad='int((nf+1)/2) * W/nf * 0.29'
+ as='int((nf+2)/2) * W/nf * 0.29' pd='2*int((nf+1)/2) * (W/nf + 0.29)' ps='2*int((nf+2)/2) * (W/nf + 0.29)'
+ nrd='0.29 / W' nrs='0.29 / W' sa=0 sb=0 sd=0 mult=3 m=3
XM85 V_CMFB_S3 PFET_GATE_10uA VDDA VDDA sky130_fd_pr__pfet_01v8 L=0.15 W=1 nf=1 ad='int((nf+1)/2) * W/nf * 0.29'
+ as='int((nf+2)/2) * W/nf * 0.29' pd='2*int((nf+1)/2) * (W/nf + 0.29)' ps='2*int((nf+2)/2) * (W/nf + 0.29)'
+ nrd='0.29 / W' nrs='0.29 / W' sa=0 sb=0 sd=0 mult=4 m=4
XM86 V_CMFB_S2 GNDA GNDA GNDA sky130_fd_pr__nfet_01v8 L=0.15 W=1 nf=1 ad='int((nf+1)/2) * W/nf * 0.29'
+ as='int((nf+2)/2) * W/nf * 0.29' pd='2*int((nf+1)/2) * (W/nf + 0.29)' ps='2*int((nf+2)/2) * (W/nf + 0.29)'
+ nrd='0.29 / W' nrs='0.29 / W' sa=0 sb=0 sd=0 mult=1 m=1
XM87 V_CMFB_S4 GNDA GNDA GNDA sky130_fd_pr__nfet_01v8 L=0.15 W=1 nf=1 ad='int((nf+1)/2) * W/nf * 0.29'
+ as='int((nf+2)/2) * W/nf * 0.29' pd='2*int((nf+1)/2) * (W/nf + 0.29)' ps='2*int((nf+2)/2) * (W/nf + 0.29)'
+ nrd='0.29 / W' nrs='0.29 / W' sa=0 sb=0 sd=0 mult=1 m=1
XM88 Vb2 GNDA GNDA GNDA sky130_fd_pr__nfet_01v8 L=0.15 W=1 nf=1 ad='int((nf+1)/2) * W/nf * 0.29' as='int((nf+2)/2) * W/nf * 0.29'
+ pd='2*int((nf+1)/2) * (W/nf + 0.29)' ps='2*int((nf+2)/2) * (W/nf + 0.29)' nrd='0.29 / W' nrs='0.29 / W'
+ sa=0 sb=0 sd=0 mult=2 m=2
XM89 V_CMFB_S1 VDDA VDDA VDDA sky130_fd_pr__pfet_01v8 L=0.15 W=1 nf=1 ad='int((nf+1)/2) * W/nf * 0.29'
+ as='int((nf+2)/2) * W/nf * 0.29' pd='2*int((nf+1)/2) * (W/nf + 0.29)' ps='2*int((nf+2)/2) * (W/nf + 0.29)'
+ nrd='0.29 / W' nrs='0.29 / W' sa=0 sb=0 sd=0 mult=2 m=2
XM90 V_CMFB_S3 VDDA VDDA VDDA sky130_fd_pr__pfet_01v8 L=0.15 W=1 nf=1 ad='int((nf+1)/2) * W/nf * 0.29'
+ as='int((nf+2)/2) * W/nf * 0.29' pd='2*int((nf+1)/2) * (W/nf + 0.29)' ps='2*int((nf+2)/2) * (W/nf + 0.29)'
+ nrd='0.29 / W' nrs='0.29 / W' sa=0 sb=0 sd=0 mult=2 m=2
XM91 Vb1 VDDA VDDA VDDA sky130_fd_pr__pfet_01v8 L=0.15 W=1 nf=1 ad='int((nf+1)/2) * W/nf * 0.29' as='int((nf+2)/2) * W/nf * 0.29'
+ pd='2*int((nf+1)/2) * (W/nf + 0.29)' ps='2*int((nf+2)/2) * (W/nf + 0.29)' nrd='0.29 / W' nrs='0.29 / W'
+ sa=0 sb=0 sd=0 mult=2 m=2
XM92 V_TOP VDDA VDDA VDDA sky130_fd_pr__pfet_01v8 L=0.15 W=2 nf=2 ad='int((nf+1)/2) * W/nf * 0.29' as='int((nf+2)/2) * W/nf * 0.29'
+ pd='2*int((nf+1)/2) * (W/nf + 0.29)' ps='2*int((nf+2)/2) * (W/nf + 0.29)' nrd='0.29 / W' nrs='0.29 / W'
+ sa=0 sb=0 sd=0 mult=1 m=1
XM93 VD4 VDDA VDDA VDDA sky130_fd_pr__pfet_01v8 L=0.2 W=7.0 nf=2 ad='int((nf+1)/2) * W/nf * 0.29' as='int((nf+2)/2) * W/nf * 0.29'
+ pd='2*int((nf+1)/2) * (W/nf + 0.29)' ps='2*int((nf+2)/2) * (W/nf + 0.29)' nrd='0.29 / W' nrs='0.29 / W'
+ sa=0 sb=0 sd=0 mult=1 m=1
XM1 Vb3 Vb2 Vb2_Vb3 Vb2_Vb3 sky130_fd_pr__pfet_01v8 L=0.2 W=3.5 nf=1 ad='int((nf+1)/2) * W/nf * 0.29'
+ as='int((nf+2)/2) * W/nf * 0.29' pd='2*int((nf+1)/2) * (W/nf + 0.29)' ps='2*int((nf+2)/2) * (W/nf + 0.29)'
+ nrd='0.29 / W' nrs='0.29 / W' sa=0 sb=0 sd=0 mult=1 m=1
XM2 Vb2_Vb3 Vb3 VDDA VDDA sky130_fd_pr__pfet_01v8 L=0.2 W=3.5 nf=1 ad='int((nf+1)/2) * W/nf * 0.29' as='int((nf+2)/2) * W/nf * 0.29'
+ pd='2*int((nf+1)/2) * (W/nf + 0.29)' ps='2*int((nf+2)/2) * (W/nf + 0.29)' nrd='0.29 / W' nrs='0.29 / W'
+ sa=0 sb=0 sd=0 mult=1 m=1
XM3 Vb2_Vb3 VDDA VDDA VDDA sky130_fd_pr__pfet_01v8 L=0.2 W=3.5 nf=2 ad='int((nf+1)/2) * W/nf * 0.29'
+ as='int((nf+2)/2) * W/nf * 0.29' pd='2*int((nf+1)/2) * (W/nf + 0.29)' ps='2*int((nf+2)/2) * (W/nf + 0.29)'
+ nrd='0.29 / W' nrs='0.29 / W' sa=0 sb=0 sd=0 mult=1 m=1
XM4 Vb3 Vb2_Vb3 Vb2_Vb3 Vb2_Vb3 sky130_fd_pr__pfet_01v8 L=0.2 W=3.5 nf=2 ad='int((nf+1)/2) * W/nf * 0.29'
+ as='int((nf+2)/2) * W/nf * 0.29' pd='2*int((nf+1)/2) * (W/nf + 0.29)' ps='2*int((nf+2)/2) * (W/nf + 0.29)'
+ nrd='0.29 / W' nrs='0.29 / W' sa=0 sb=0 sd=0 mult=1 m=1
XM94 Vb2 Vb2 Vb2_2 Vb2_2 sky130_fd_pr__pfet_01v8 L=0.2 W=3.5 nf=1 ad='int((nf+1)/2) * W/nf * 0.29' as='int((nf+2)/2) * W/nf * 0.29'
+ pd='2*int((nf+1)/2) * (W/nf + 0.29)' ps='2*int((nf+2)/2) * (W/nf + 0.29)' nrd='0.29 / W' nrs='0.29 / W'
+ sa=0 sb=0 sd=0 mult=1 m=1
XM95 Vb2_2 Vb2 VDDA VDDA sky130_fd_pr__pfet_01v8 L=0.2 W=1.8 nf=1 ad='int((nf+1)/2) * W/nf * 0.29' as='int((nf+2)/2) * W/nf * 0.29'
+ pd='2*int((nf+1)/2) * (W/nf + 0.29)' ps='2*int((nf+2)/2) * (W/nf + 0.29)' nrd='0.29 / W' nrs='0.29 / W'
+ sa=0 sb=0 sd=0 mult=1 m=1
XM96 Vb2_2 VDDA VDDA VDDA sky130_fd_pr__pfet_01v8 L=0.2 W=1.8 nf=2 ad='int((nf+1)/2) * W/nf * 0.29' as='int((nf+2)/2) * W/nf * 0.29'
+ pd='2*int((nf+1)/2) * (W/nf + 0.29)' ps='2*int((nf+2)/2) * (W/nf + 0.29)' nrd='0.29 / W' nrs='0.29 / W'
+ sa=0 sb=0 sd=0 mult=1 m=1
XM97 Vb2 Vb2_2 Vb2_2 Vb2_2 sky130_fd_pr__pfet_01v8 L=0.2 W=3.5 nf=2 ad='int((nf+1)/2) * W/nf * 0.29'
+ as='int((nf+2)/2) * W/nf * 0.29' pd='2*int((nf+1)/2) * (W/nf + 0.29)' ps='2*int((nf+2)/2) * (W/nf + 0.29)'
+ nrd='0.29 / W' nrs='0.29 / W' sa=0 sb=0 sd=0 mult=1 m=1
XM5 VDDA VDDA VDDA VDDA sky130_fd_pr__pfet_01v8 L=0.2 W=3.5 nf=2 ad='int((nf+1)/2) * W/nf * 0.29' as='int((nf+2)/2) * W/nf * 0.29'
+ pd='2*int((nf+1)/2) * (W/nf + 0.29)' ps='2*int((nf+2)/2) * (W/nf + 0.29)' nrd='0.29 / W' nrs='0.29 / W'
+ sa=0 sb=0 sd=0 mult=1 m=1
XM6 Vb2_Vb3 Vb2_Vb3 Vb2_Vb3 Vb2_Vb3 sky130_fd_pr__pfet_01v8 L=0.2 W=3.5 nf=2 ad='int((nf+1)/2) * W/nf * 0.29'
+ as='int((nf+2)/2) * W/nf * 0.29' pd='2*int((nf+1)/2) * (W/nf + 0.29)' ps='2*int((nf+2)/2) * (W/nf + 0.29)'
+ nrd='0.29 / W' nrs='0.29 / W' sa=0 sb=0 sd=0 mult=1 m=1
XM43 VDDA VDDA VDDA VDDA sky130_fd_pr__pfet_01v8 L=0.2 W=1.8 nf=2 ad='int((nf+1)/2) * W/nf * 0.29' as='int((nf+2)/2) * W/nf * 0.29'
+ pd='2*int((nf+1)/2) * (W/nf + 0.29)' ps='2*int((nf+2)/2) * (W/nf + 0.29)' nrd='0.29 / W' nrs='0.29 / W'
+ sa=0 sb=0 sd=0 mult=1 m=1
XM98 Vb2_2 Vb2_2 Vb2_2 Vb2_2 sky130_fd_pr__pfet_01v8 L=0.2 W=3.5 nf=2 ad='int((nf+1)/2) * W/nf * 0.29'
+ as='int((nf+2)/2) * W/nf * 0.29' pd='2*int((nf+1)/2) * (W/nf + 0.29)' ps='2*int((nf+2)/2) * (W/nf + 0.29)'
+ nrd='0.29 / W' nrs='0.29 / W' sa=0 sb=0 sd=0 mult=1 m=1
.ends


* expanding   symbol:
*+  /foss/designs/my_design/projects/bandgapref/xschem_ngspice/new_files/opamp_bandgap_2.sym # of pins=5
** sym_path: projects/bandgapref/xschem_ngspice/new_files/opamp_bandgap_2.sym
** sch_path: projects/bandgapref/xschem_ngspice/new_files/opamp_bandgap_2.sch
.subckt opamp_bandgap_2 VDDA Vout Vin- Vin+ GNDA
*.ipin Vin+
*.opin Vout
*.ipin Vin-
*.ipin GNDA
*.ipin VDDA
XM1 V_p VDDA GNDA GNDA sky130_fd_pr__nfet_01v8 L=10 W=5 nf=1 ad='int((nf+1)/2) * W/nf * 0.29' as='int((nf+2)/2) * W/nf * 0.29'
+ pd='2*int((nf+1)/2) * (W/nf + 0.29)' ps='2*int((nf+2)/2) * (W/nf + 0.29)' nrd='0.29 / W' nrs='0.29 / W'
+ sa=0 sb=0 sd=0 mult=1 m=1
XM2 V_mirror Vin- V_p GNDA sky130_fd_pr__nfet_01v8 L=0.2 W=5 nf=1 ad='int((nf+1)/2) * W/nf * 0.29' as='int((nf+2)/2) * W/nf * 0.29'
+ pd='2*int((nf+1)/2) * (W/nf + 0.29)' ps='2*int((nf+2)/2) * (W/nf + 0.29)' nrd='0.29 / W' nrs='0.29 / W'
+ sa=0 sb=0 sd=0 mult=1 m=1
XM3 1st_Vout Vin+ V_p GNDA sky130_fd_pr__nfet_01v8 L=0.2 W=5 nf=1 ad='int((nf+1)/2) * W/nf * 0.29' as='int((nf+2)/2) * W/nf * 0.29'
+ pd='2*int((nf+1)/2) * (W/nf + 0.29)' ps='2*int((nf+2)/2) * (W/nf + 0.29)' nrd='0.29 / W' nrs='0.29 / W'
+ sa=0 sb=0 sd=0 mult=1 m=1
XM5 V_mirror V_mirror VDDA VDDA sky130_fd_pr__pfet_01v8 L=0.2 W=10 nf=2 ad='int((nf+1)/2) * W/nf * 0.29'
+ as='int((nf+2)/2) * W/nf * 0.29' pd='2*int((nf+1)/2) * (W/nf + 0.29)' ps='2*int((nf+2)/2) * (W/nf + 0.29)'
+ nrd='0.29 / W' nrs='0.29 / W' sa=0 sb=0 sd=0 mult=1 m=1
XM6 1st_Vout V_mirror VDDA VDDA sky130_fd_pr__pfet_01v8 L=0.2 W=10 nf=2 ad='int((nf+1)/2) * W/nf * 0.29'
+ as='int((nf+2)/2) * W/nf * 0.29' pd='2*int((nf+1)/2) * (W/nf + 0.29)' ps='2*int((nf+2)/2) * (W/nf + 0.29)'
+ nrd='0.29 / W' nrs='0.29 / W' sa=0 sb=0 sd=0 mult=1 m=1
XM4 Vout VDDA GNDA GNDA sky130_fd_pr__nfet_01v8 L=10 W=5 nf=1 ad='int((nf+1)/2) * W/nf * 0.29' as='int((nf+2)/2) * W/nf * 0.29'
+ pd='2*int((nf+1)/2) * (W/nf + 0.29)' ps='2*int((nf+2)/2) * (W/nf + 0.29)' nrd='0.29 / W' nrs='0.29 / W'
+ sa=0 sb=0 sd=0 mult=1 m=1
XM7 Vout 1st_Vout VDDA VDDA sky130_fd_pr__pfet_01v8 L=0.2 W=10 nf=2 ad='int((nf+1)/2) * W/nf * 0.29'
+ as='int((nf+2)/2) * W/nf * 0.29' pd='2*int((nf+1)/2) * (W/nf + 0.29)' ps='2*int((nf+2)/2) * (W/nf + 0.29)'
+ nrd='0.29 / W' nrs='0.29 / W' sa=0 sb=0 sd=0 mult=1 m=1
.ends

.GLOBAL GND
.GLOBAL VDD
.end
